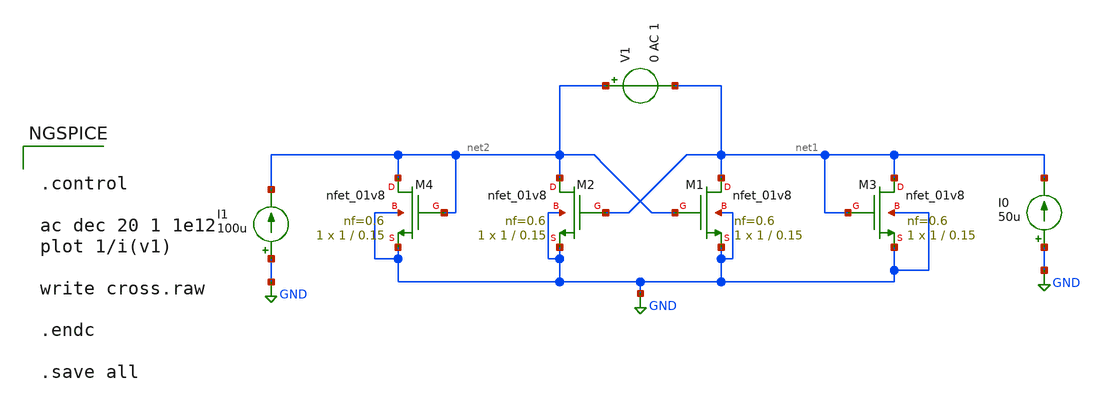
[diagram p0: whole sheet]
** sch_path: cross.sch
**.subckt cross
XM1 net1 net2 GND GND sky130_fd_pr__nfet_01v8 L=0.15 W=1 nf=0.6 ad='int((nf+1)/2) * W/nf * 0.29' as='int((nf+2)/2) * W/nf * 0.29'
+ pd='2*int((nf+1)/2) * (W/nf + 0.29)' ps='2*int((nf+2)/2) * (W/nf + 0.29)' nrd='0.29 / W' nrs='0.29 / W'
+ sa=0 sb=0 sd=0 mult=1 m=1
XM2 net2 net1 GND GND sky130_fd_pr__nfet_01v8 L=0.15 W=1 nf=0.6 ad='int((nf+1)/2) * W/nf * 0.29' as='int((nf+2)/2) * W/nf * 0.29'
+ pd='2*int((nf+1)/2) * (W/nf + 0.29)' ps='2*int((nf+2)/2) * (W/nf + 0.29)' nrd='0.29 / W' nrs='0.29 / W'
+ sa=0 sb=0 sd=0 mult=1 m=1
XM3 net1 net1 GND GND sky130_fd_pr__nfet_01v8 L=0.15 W=1 nf=0.6 ad='int((nf+1)/2) * W/nf * 0.29' as='int((nf+2)/2) * W/nf * 0.29'
+ pd='2*int((nf+1)/2) * (W/nf + 0.29)' ps='2*int((nf+2)/2) * (W/nf + 0.29)' nrd='0.29 / W' nrs='0.29 / W'
+ sa=0 sb=0 sd=0 mult=1 m=1
XM4 net2 net2 GND GND sky130_fd_pr__nfet_01v8 L=0.15 W=1 nf=0.6 ad='int((nf+1)/2) * W/nf * 0.29' as='int((nf+2)/2) * W/nf * 0.29'
+ pd='2*int((nf+1)/2) * (W/nf + 0.29)' ps='2*int((nf+2)/2) * (W/nf + 0.29)' nrd='0.29 / W' nrs='0.29 / W'
+ sa=0 sb=0 sd=0 mult=1 m=1
V1 net2 net1 0 AC 1
I0 GND net1 50u
I1 GND net2 100u
**** begin user architecture code


.control

ac dec 20 1 1e12
plot 1/i(v1)

write cross.raw

.endc

.save all



** opencircuitdesign pdks install
.lib $::SKYWATER_MODELS/sky130.lib.spice tt


**** end user architecture code
**.ends
.GLOBAL GND
.end
